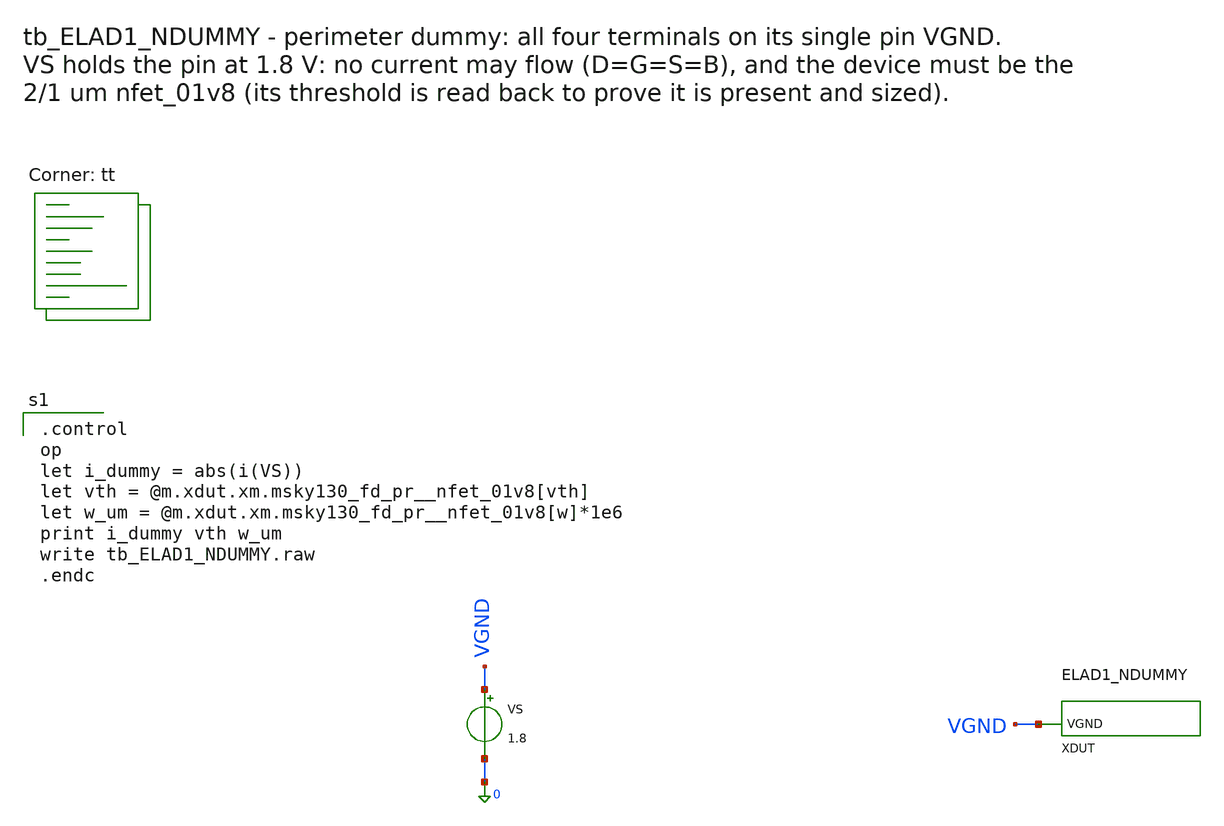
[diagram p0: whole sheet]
** sch_path: cells/ELAD1_NDUMMY/schematic/tb_ELAD1_NDUMMY.sch
**.subckt tb_ELAD1_NDUMMY
VS VGND 0 1.8
XDUT VGND ELAD1_NDUMMY
**** begin user architecture code

.control
op
let i_dummy = abs(i(VS))
let vth = @m.xdut.xm.msky130_fd_pr__nfet_01v8[vth]
let w_um = @m.xdut.xm.msky130_fd_pr__nfet_01v8[w]*1e6
print i_dummy vth w_um
write tb_ELAD1_NDUMMY.raw
.endc

.lib $::SKYWATER_MODELS/sky130.lib.spice tt
**** end user architecture code
**.ends

* expanding   symbol:  ELAD1_NDUMMY.sym # of pins=1
** sym_path: cells/ELAD1_NDUMMY/schematic/ELAD1_NDUMMY.sym
** sch_path: cells/ELAD1_NDUMMY/schematic/ELAD1_NDUMMY.sch
.subckt ELAD1_NDUMMY VGND
*.iopin VGND
XM VGND VGND VGND VGND sky130_fd_pr__nfet_01v8 L=1 W=2 nf=1 ad='int((1 + 1)/2) * 2 / 1 * 0.29' as='int((1 + 2)/2) * 2 / 1 * 0.29'
+ pd='2*int((1 + 1)/2) * (2 / 1 + 0.29)' ps='2*int((1 + 2)/2) * (2 / 1 + 0.29)' nrd='0.29 / 2 ' nrs='0.29 / 2 '
+ sa=0 sb=0 sd=0 mult=1 m=1
.ends

.end
